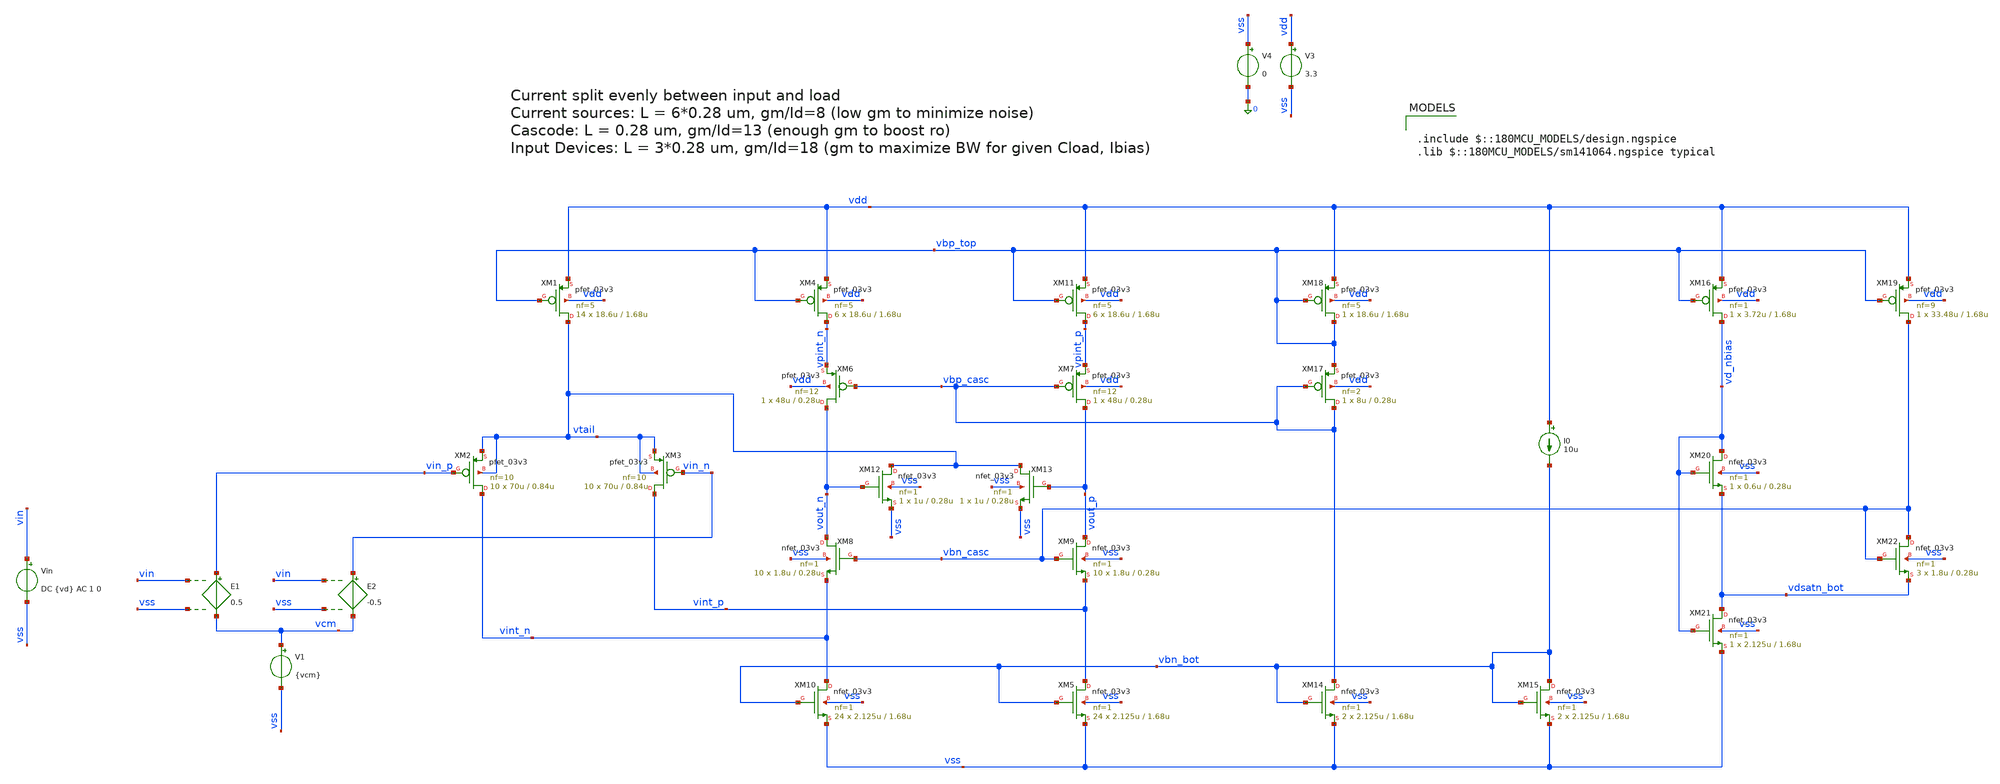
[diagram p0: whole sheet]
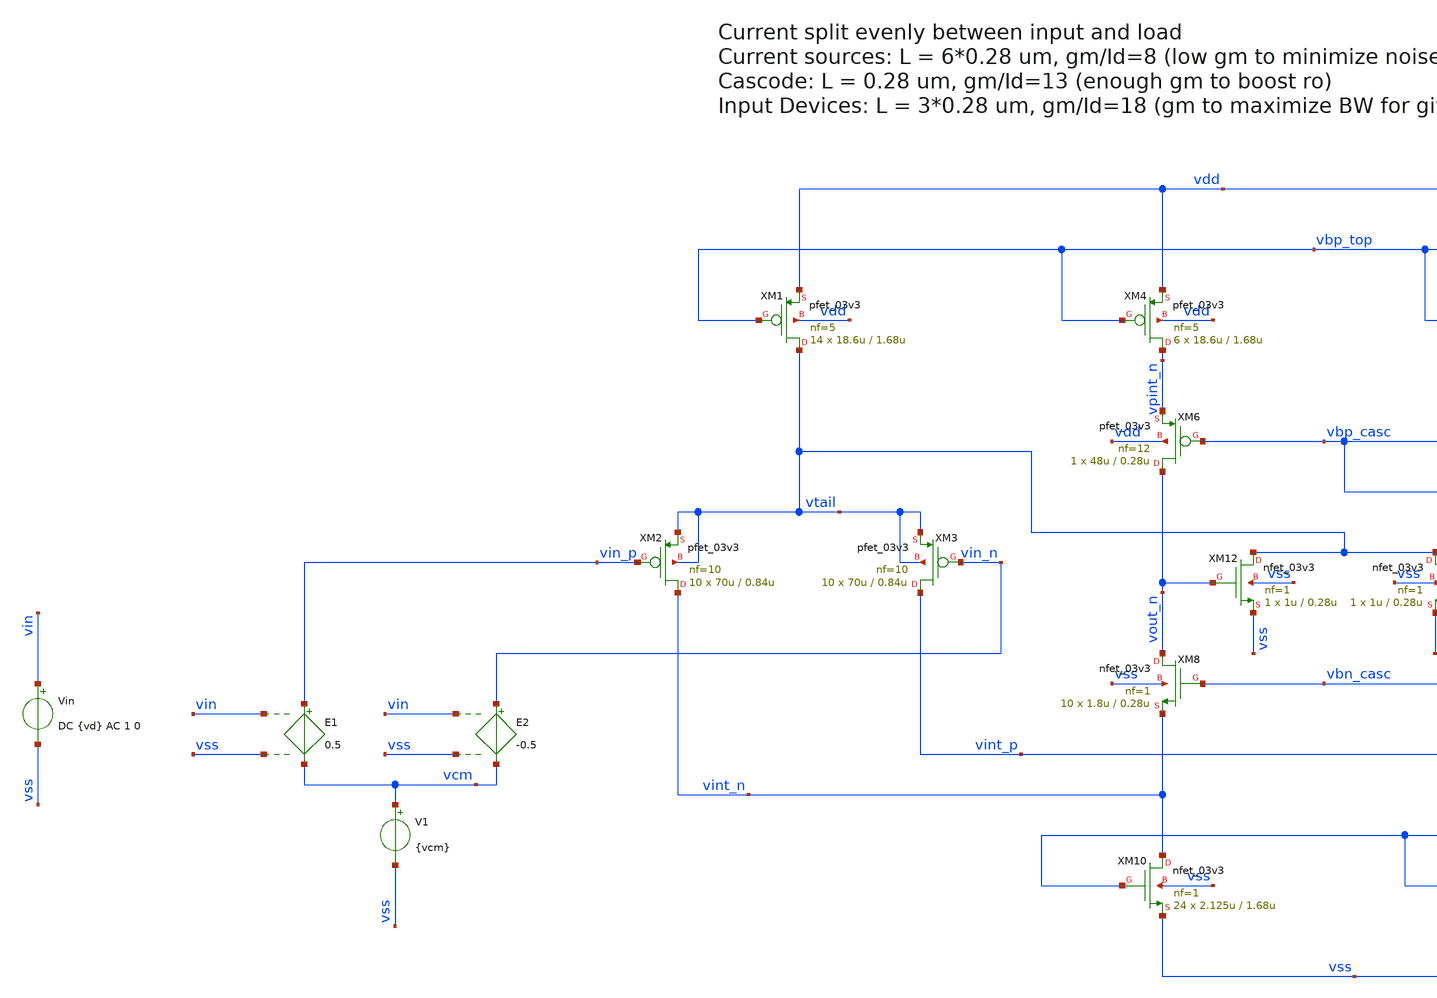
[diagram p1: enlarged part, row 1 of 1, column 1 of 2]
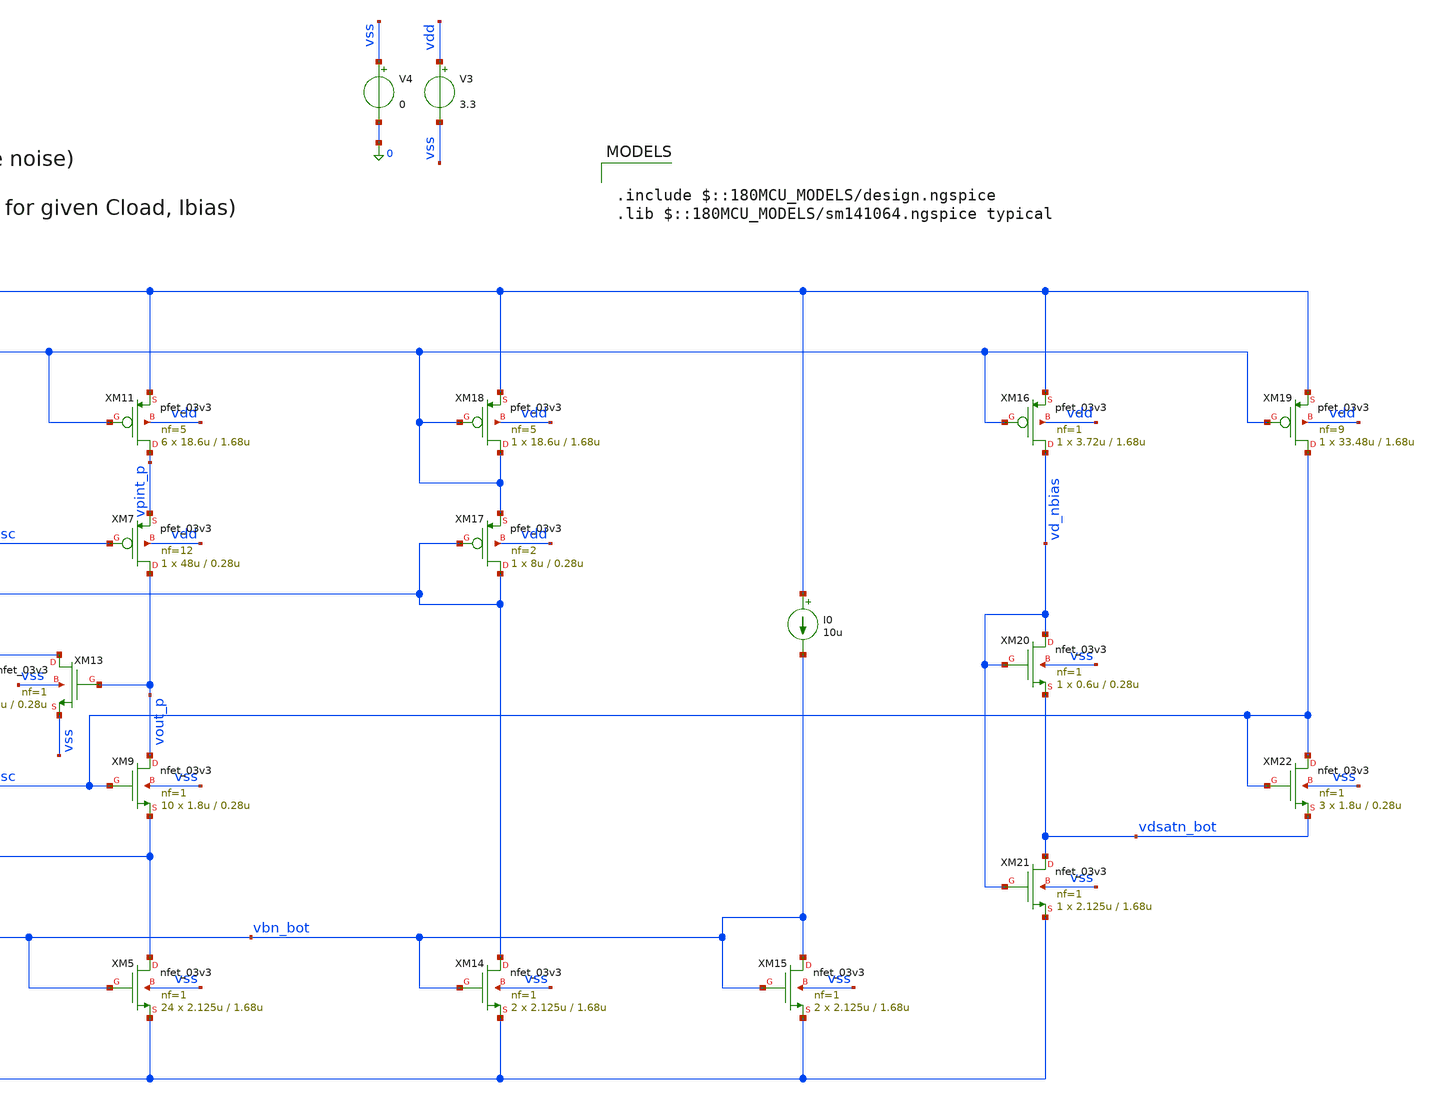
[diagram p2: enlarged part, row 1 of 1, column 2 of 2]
** sch_path: xschem/ota/folded_cascode_test.sch
**.subckt folded_cascode_test
XM2 vint_n vin_p vtail vtail pfet_03v3 L=0.84u W=70u nf=10 ad='int((nf+1)/2) * W/nf * 0.18u' as='int((nf+2)/2) * W/nf * 0.18u'
+ pd='2*int((nf+1)/2) * (W/nf + 0.18u)' ps='2*int((nf+2)/2) * (W/nf + 0.18u)' nrd='0.18u / W' nrs='0.18u / W'
+ sa=0 sb=0 sd=0 m=10
XM1 vtail vbp_top vdd vdd pfet_03v3 L=1.68u W=18.6u nf=5 ad='int((nf+1)/2) * W/nf * 0.18u' as='int((nf+2)/2) * W/nf * 0.18u'
+ pd='2*int((nf+1)/2) * (W/nf + 0.18u)' ps='2*int((nf+2)/2) * (W/nf + 0.18u)' nrd='0.18u / W' nrs='0.18u / W'
+ sa=0 sb=0 sd=0 m=14
XM6 vout_n vbp_casc vpint_n vdd pfet_03v3 L=0.28u W=48u nf=12 ad='int((nf+1)/2) * W/nf * 0.18u' as='int((nf+2)/2) * W/nf * 0.18u'
+ pd='2*int((nf+1)/2) * (W/nf + 0.18u)' ps='2*int((nf+2)/2) * (W/nf + 0.18u)' nrd='0.18u / W' nrs='0.18u / W'
+ sa=0 sb=0 sd=0 m=1
XM12 vtail vout_n vss vss nfet_03v3 L=0.28u W=1u nf=1 ad='int((nf+1)/2) * W/nf * 0.18u' as='int((nf+2)/2) * W/nf * 0.18u'
+ pd='2*int((nf+1)/2) * (W/nf + 0.18u)' ps='2*int((nf+2)/2) * (W/nf + 0.18u)' nrd='0.18u / W' nrs='0.18u / W'
+ sa=0 sb=0 sd=0 m=1
XM9 vout_p vbn_casc vint_p vss nfet_03v3 L=0.28u W=1.8u nf=1 ad='int((nf+1)/2) * W/nf * 0.18u' as='int((nf+2)/2) * W/nf * 0.18u'
+ pd='2*int((nf+1)/2) * (W/nf + 0.18u)' ps='2*int((nf+2)/2) * (W/nf + 0.18u)' nrd='0.18u / W' nrs='0.18u / W'
+ sa=0 sb=0 sd=0 m=10
XM7 vout_p vbp_casc vpint_p vdd pfet_03v3 L=0.28u W=48u nf=12 ad='int((nf+1)/2) * W/nf * 0.18u' as='int((nf+2)/2) * W/nf * 0.18u'
+ pd='2*int((nf+1)/2) * (W/nf + 0.18u)' ps='2*int((nf+2)/2) * (W/nf + 0.18u)' nrd='0.18u / W' nrs='0.18u / W'
+ sa=0 sb=0 sd=0 m=1
XM14 vbp_casc vbn_bot vss vss nfet_03v3 L=1.68u W=2.125u nf=1 ad='int((nf+1)/2) * W/nf * 0.18u' as='int((nf+2)/2) * W/nf * 0.18u'
+ pd='2*int((nf+1)/2) * (W/nf + 0.18u)' ps='2*int((nf+2)/2) * (W/nf + 0.18u)' nrd='0.18u / W' nrs='0.18u / W'
+ sa=0 sb=0 sd=0 m=2
XM15 vbn_bot vbn_bot vss vss nfet_03v3 L=1.68u W=2.125u nf=1 ad='int((nf+1)/2) * W/nf * 0.18u' as='int((nf+2)/2) * W/nf * 0.18u'
+ pd='2*int((nf+1)/2) * (W/nf + 0.18u)' ps='2*int((nf+2)/2) * (W/nf + 0.18u)' nrd='0.18u / W' nrs='0.18u / W'
+ sa=0 sb=0 sd=0 m=2
I0 vdd vbn_bot 10u
XM17 vbp_casc vbp_casc vbp_top vdd pfet_03v3 L=0.28u W=8u nf=2 ad='int((nf+1)/2) * W/nf * 0.18u' as='int((nf+2)/2) * W/nf * 0.18u'
+ pd='2*int((nf+1)/2) * (W/nf + 0.18u)' ps='2*int((nf+2)/2) * (W/nf + 0.18u)' nrd='0.18u / W' nrs='0.18u / W'
+ sa=0 sb=0 sd=0 m=1
XM18 vbp_top vbp_top vdd vdd pfet_03v3 L=1.68u W=18.6u nf=5 ad='int((nf+1)/2) * W/nf * 0.18u' as='int((nf+2)/2) * W/nf * 0.18u'
+ pd='2*int((nf+1)/2) * (W/nf + 0.18u)' ps='2*int((nf+2)/2) * (W/nf + 0.18u)' nrd='0.18u / W' nrs='0.18u / W'
+ sa=0 sb=0 sd=0 m=1
V3 vdd vss 3.3
V4 vss 0 0
V1 vcm vss {vcm}
XM3 vint_p vin_n vtail vtail pfet_03v3 L=0.84u W=70u nf=10 ad='int((nf+1)/2) * W/nf * 0.18u' as='int((nf+2)/2) * W/nf * 0.18u'
+ pd='2*int((nf+1)/2) * (W/nf + 0.18u)' ps='2*int((nf+2)/2) * (W/nf + 0.18u)' nrd='0.18u / W' nrs='0.18u / W'
+ sa=0 sb=0 sd=0 m=10
XM4 vpint_n vbp_top vdd vdd pfet_03v3 L=1.68u W=18.6u nf=5 ad='int((nf+1)/2) * W/nf * 0.18u' as='int((nf+2)/2) * W/nf * 0.18u'
+ pd='2*int((nf+1)/2) * (W/nf + 0.18u)' ps='2*int((nf+2)/2) * (W/nf + 0.18u)' nrd='0.18u / W' nrs='0.18u / W'
+ sa=0 sb=0 sd=0 m=6
XM11 vpint_p vbp_top vdd vdd pfet_03v3 L=1.68u W=18.6u nf=5 ad='int((nf+1)/2) * W/nf * 0.18u' as='int((nf+2)/2) * W/nf * 0.18u'
+ pd='2*int((nf+1)/2) * (W/nf + 0.18u)' ps='2*int((nf+2)/2) * (W/nf + 0.18u)' nrd='0.18u / W' nrs='0.18u / W'
+ sa=0 sb=0 sd=0 m=6
XM10 vint_n vbn_bot vss vss nfet_03v3 L=1.68u W=2.125u nf=1 ad='int((nf+1)/2) * W/nf * 0.18u' as='int((nf+2)/2) * W/nf * 0.18u'
+ pd='2*int((nf+1)/2) * (W/nf + 0.18u)' ps='2*int((nf+2)/2) * (W/nf + 0.18u)' nrd='0.18u / W' nrs='0.18u / W'
+ sa=0 sb=0 sd=0 m=24
XM13 vtail vout_p vss vss nfet_03v3 L=0.28u W=1u nf=1 ad='int((nf+1)/2) * W/nf * 0.18u' as='int((nf+2)/2) * W/nf * 0.18u'
+ pd='2*int((nf+1)/2) * (W/nf + 0.18u)' ps='2*int((nf+2)/2) * (W/nf + 0.18u)' nrd='0.18u / W' nrs='0.18u / W'
+ sa=0 sb=0 sd=0 m=1
XM16 vd_nbias vbp_top vdd vdd pfet_03v3 L=1.68u W=3.72u nf=1 ad='int((nf+1)/2) * W/nf * 0.18u' as='int((nf+2)/2) * W/nf * 0.18u'
+ pd='2*int((nf+1)/2) * (W/nf + 0.18u)' ps='2*int((nf+2)/2) * (W/nf + 0.18u)' nrd='0.18u / W' nrs='0.18u / W'
+ sa=0 sb=0 sd=0 m=1
XM19 vbn_casc vbp_top vdd vdd pfet_03v3 L=1.68u W=33.48u nf=9 ad='int((nf+1)/2) * W/nf * 0.18u' as='int((nf+2)/2) * W/nf * 0.18u'
+ pd='2*int((nf+1)/2) * (W/nf + 0.18u)' ps='2*int((nf+2)/2) * (W/nf + 0.18u)' nrd='0.18u / W' nrs='0.18u / W'
+ sa=0 sb=0 sd=0 m=1
XM22 vbn_casc vbn_casc vdsatn_bot vss nfet_03v3 L=0.28u W=1.8u nf=1 ad='int((nf+1)/2) * W/nf * 0.18u'
+ as='int((nf+2)/2) * W/nf * 0.18u' pd='2*int((nf+1)/2) * (W/nf + 0.18u)' ps='2*int((nf+2)/2) * (W/nf + 0.18u)'
+ nrd='0.18u / W' nrs='0.18u / W' sa=0 sb=0 sd=0 m=3
XM21 vdsatn_bot vd_nbias vss vss nfet_03v3 L=1.68u W=2.125u nf=1 ad='int((nf+1)/2) * W/nf * 0.18u' as='int((nf+2)/2) * W/nf * 0.18u'
+ pd='2*int((nf+1)/2) * (W/nf + 0.18u)' ps='2*int((nf+2)/2) * (W/nf + 0.18u)' nrd='0.18u / W' nrs='0.18u / W'
+ sa=0 sb=0 sd=0 m=1
XM5 vint_p vbn_bot vss vss nfet_03v3 L=1.68u W=2.125u nf=1 ad='int((nf+1)/2) * W/nf * 0.18u' as='int((nf+2)/2) * W/nf * 0.18u'
+ pd='2*int((nf+1)/2) * (W/nf + 0.18u)' ps='2*int((nf+2)/2) * (W/nf + 0.18u)' nrd='0.18u / W' nrs='0.18u / W'
+ sa=0 sb=0 sd=0 m=24
XM8 vout_n vbn_casc vint_n vss nfet_03v3 L=0.28u W=1.8u nf=1 ad='int((nf+1)/2) * W/nf * 0.18u' as='int((nf+2)/2) * W/nf * 0.18u'
+ pd='2*int((nf+1)/2) * (W/nf + 0.18u)' ps='2*int((nf+2)/2) * (W/nf + 0.18u)' nrd='0.18u / W' nrs='0.18u / W'
+ sa=0 sb=0 sd=0 m=10
XM20 vd_nbias vd_nbias vdsatn_bot vss nfet_03v3 L=0.28u W=0.6u nf=1 ad='int((nf+1)/2) * W/nf * 0.18u'
+ as='int((nf+2)/2) * W/nf * 0.18u' pd='2*int((nf+1)/2) * (W/nf + 0.18u)' ps='2*int((nf+2)/2) * (W/nf + 0.18u)'
+ nrd='0.18u / W' nrs='0.18u / W' sa=0 sb=0 sd=0 m=1
E1 vin_p vcm vin vss 0.5
E2 vin_n vcm vin vss -0.5
Vin vin vss DC {vd} AC 1 0
**** begin user architecture code

.param vcm=0.5
.param vd=0
.control
save @m.xm1.m0[id] @m.xm2.m0[id] @m.xm3.m0[id] @m.xm4.m0[id] @m.xm5.m0[id]
save @m.xm6.m0[id] @m.xm7.m0[id] @m.xm8.m0[id] @m.xm9.m0[id] @m.xm10.m0[id]
save @m.xm11.m0[id] @m.xm12.m0[id] @m.xm13.m0[id] @m.xm14.m0[id] @m.xm15.m0[id]
save @m.xm16.m0[id] @m.xm17.m0[id] @m.xm18.m0[id] @m.xm19.m0[id] @m.xm20.m0[id]
save @m.xm21.m0[id] @m.xm22.m0[id]

save @m.xm1.m0[gm] @m.xm2.m0[gm] @m.xm3.m0[gm] @m.xm4.m0[gm] @m.xm5.m0[gm]
save @m.xm6.m0[gm] @m.xm7.m0[gm] @m.xm8.m0[gm] @m.xm9.m0[gm] @m.xm10.m0[gm]
save @m.xm11.m0[gm] @m.xm12.m0[gm] @m.xm13.m0[gm] @m.xm14.m0[gm] @m.xm15.m0[gm]
save @m.xm16.m0[gm] @m.xm17.m0[gm] @m.xm18.m0[gm] @m.xm19.m0[gm] @m.xm20.m0[gm]
save @m.xm21.m0[gm] @m.xm22.m0[gm]

save all
op
write results_op.raw all
noise v(vout_p, vout_n) Vin dec 10 1 1000Meg
.endc


.include $::180MCU_MODELS/design.ngspice
.lib $::180MCU_MODELS/sm141064.ngspice typical

**** end user architecture code
**.ends
.end
